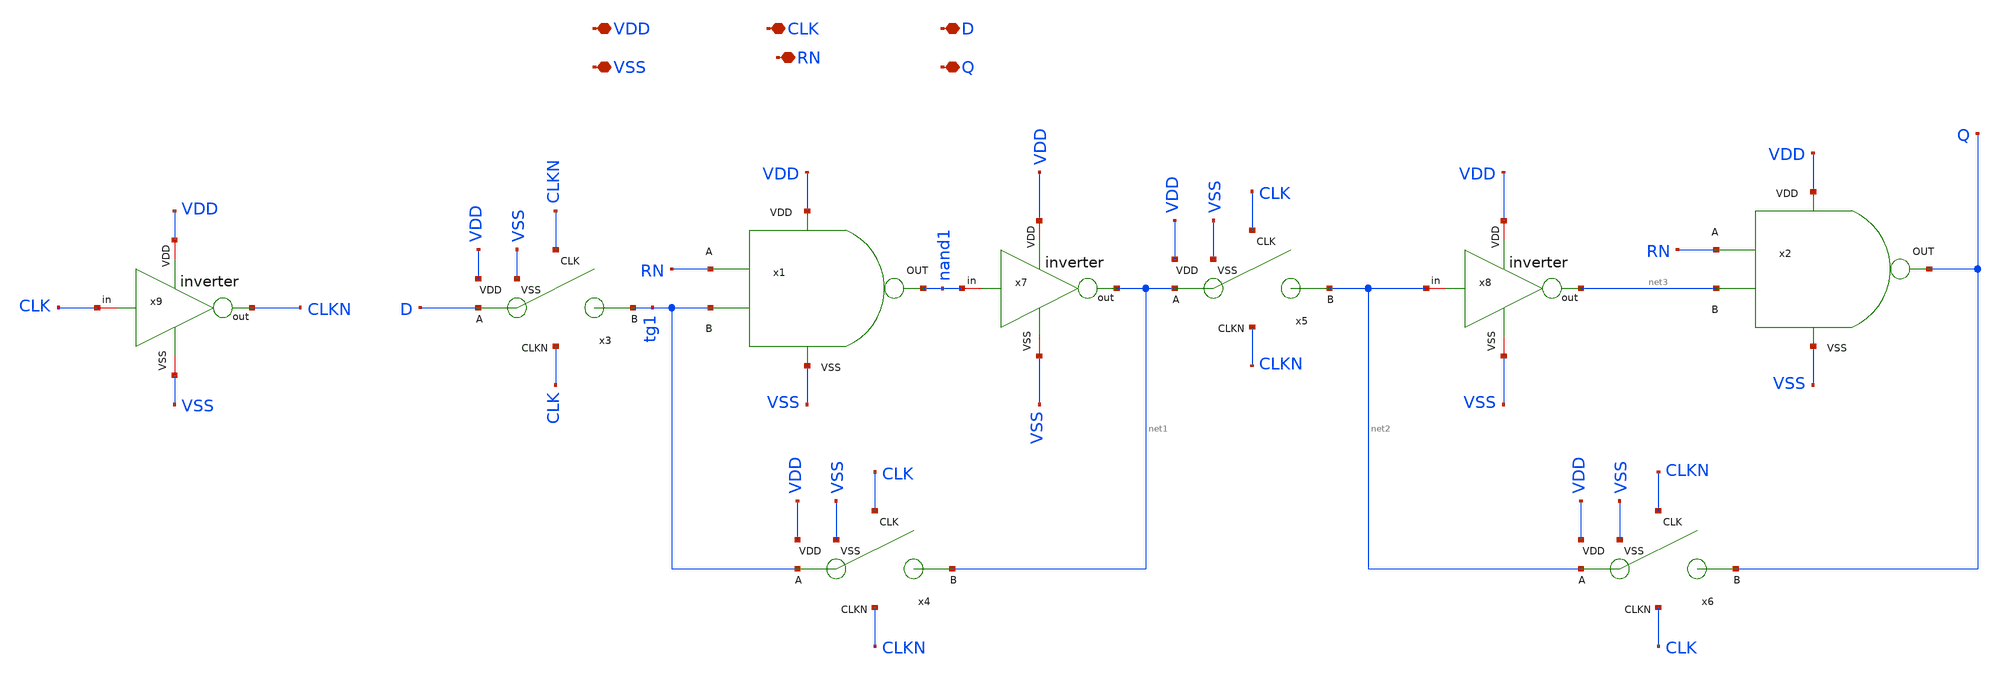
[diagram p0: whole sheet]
** sch_path: designs/sar_adc/digital/flip_flop/xschem/FF_D.sch
**.subckt FF_D VDD VSS CLK D RN Q
*.iopin VDD
*.iopin VSS
*.iopin CLK
*.iopin D
*.iopin RN
*.iopin Q
x1 VDD VSS RN tg1 nand1 NAND
x2 VDD VSS RN net3 Q NAND
x3 CLKN D VDD tg1 CLK VSS TG
x4 CLK tg1 VDD net1 CLKN VSS TG
x5 CLK net1 VDD net2 CLKN VSS TG
x6 CLKN net2 VDD Q CLK VSS TG
x7 VDD nand1 net1 VSS inverter
x8 VDD net2 net3 VSS inverter
x9 VDD CLK CLKN VSS inverter
**.ends

* expanding   symbol:  designs/sar_adc/digital/NAND/xschem/NAND.sym # of pins=5
** sym_path: designs/sar_adc/digital/NAND/xschem/NAND.sym
** sch_path: designs/sar_adc/digital/NAND/xschem/NAND.sch
.subckt NAND VDD VSS A B out
*.iopin VDD
*.iopin A
*.iopin B
*.iopin out
*.iopin VSS
XM2 net1 A VDD VDD pfet_03v3 L=0.28u W=0.5u nf=1 ad='int((nf+1)/2) * W/nf * 0.18u' as='int((nf+2)/2) * W/nf * 0.18u'
+ pd='2*int((nf+1)/2) * (W/nf + 0.18u)' ps='2*int((nf+2)/2) * (W/nf + 0.18u)' nrd='0.18u / W' nrs='0.18u / W'
+ sa=0 sb=0 sd=0 m=2
XM1 net1 A net3 VSS nfet_03v3 L=0.28u W=0.5u nf=1 ad='int((nf+1)/2) * W/nf * 0.18u' as='int((nf+2)/2) * W/nf * 0.18u'
+ pd='2*int((nf+1)/2) * (W/nf + 0.18u)' ps='2*int((nf+2)/2) * (W/nf + 0.18u)' nrd='0.18u / W' nrs='0.18u / W'
+ sa=0 sb=0 sd=0 m=1
XM3 net1 B VDD VDD pfet_03v3 L=0.28u W=0.5u nf=1 ad='int((nf+1)/2) * W/nf * 0.18u' as='int((nf+2)/2) * W/nf * 0.18u'
+ pd='2*int((nf+1)/2) * (W/nf + 0.18u)' ps='2*int((nf+2)/2) * (W/nf + 0.18u)' nrd='0.18u / W' nrs='0.18u / W'
+ sa=0 sb=0 sd=0 m=2
XM4 net3 B VSS VSS nfet_03v3 L=0.28u W=0.5u nf=1 ad='int((nf+1)/2) * W/nf * 0.18u' as='int((nf+2)/2) * W/nf * 0.18u'
+ pd='2*int((nf+1)/2) * (W/nf + 0.18u)' ps='2*int((nf+2)/2) * (W/nf + 0.18u)' nrd='0.18u / W' nrs='0.18u / W'
+ sa=0 sb=0 sd=0 m=1
x1 VDD net1 net2 VSS inverter
x2 VDD net2 out VSS inverter
.ends


* expanding   symbol:  designs/sar_adc/digital/TG/xschem/TG.sym # of pins=6
** sym_path: designs/sar_adc/digital/TG/xschem/TG.sym
** sch_path: designs/sar_adc/digital/TG/xschem/TG.sch
.subckt TG CLK A VDD B CLKN VSS
*.iopin VDD
*.iopin VSS
*.ipin CLK
*.ipin CLKN
*.iopin A
*.iopin B
XM1 A CLK B VSS nfet_03v3 L=0.28u W=0.22u nf=1 ad='int((nf+1)/2) * W/nf * 0.18u' as='int((nf+2)/2) * W/nf * 0.18u'
+ pd='2*int((nf+1)/2) * (W/nf + 0.18u)' ps='2*int((nf+2)/2) * (W/nf + 0.18u)' nrd='0.18u / W' nrs='0.18u / W'
+ sa=0 sb=0 sd=0 m=1
XM2 A CLKN B VDD pfet_03v3 L=0.28u W=0.22u nf=1 ad='int((nf+1)/2) * W/nf * 0.18u' as='int((nf+2)/2) * W/nf * 0.18u'
+ pd='2*int((nf+1)/2) * (W/nf + 0.18u)' ps='2*int((nf+2)/2) * (W/nf + 0.18u)' nrd='0.18u / W' nrs='0.18u / W'
+ sa=0 sb=0 sd=0 m=1
.ends


* expanding   symbol:  designs/sar_adc/digital/buffer_inv_x1/xschem/inverter.sym # of pins=6
** sym_path: designs/sar_adc/digital/buffer_inv_x1/xschem/inverter.sym
** sch_path: designs/sar_adc/digital/buffer_inv_x1/xschem/inverter.sch
.subckt inverter VDD in out VSS
*.opin out
*.iopin in
*.iopin VDD
*.iopin VSS
XM1 out in VSS VSS nfet_03v3 L=0.56u W=0.25u nf=1 ad='int((nf+1)/2) * W/nf * 0.18u' as='int((nf+2)/2) * W/nf * 0.18u'
+ pd='2*int((nf+1)/2) * (W/nf + 0.18u)' ps='2*int((nf+2)/2) * (W/nf + 0.18u)' nrd='0.18u / W' nrs='0.18u / W'
+ sa=0 sb=0 sd=0 m=2
XM2 out in VDD VDD pfet_03v3 L=0.56u W=0.25u nf=1 ad='int((nf+1)/2) * W/nf * 0.18u' as='int((nf+2)/2) * W/nf * 0.18u'
+ pd='2*int((nf+1)/2) * (W/nf + 0.18u)' ps='2*int((nf+2)/2) * (W/nf + 0.18u)' nrd='0.18u / W' nrs='0.18u / W'
+ sa=0 sb=0 sd=0 m=4
.ends

.end
